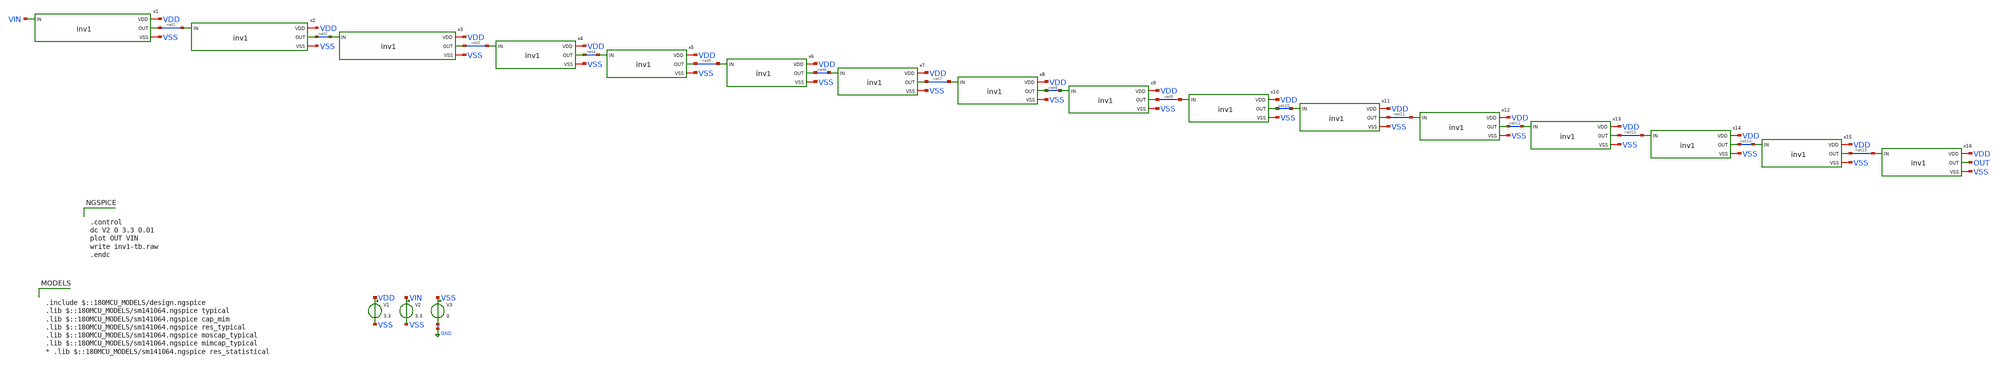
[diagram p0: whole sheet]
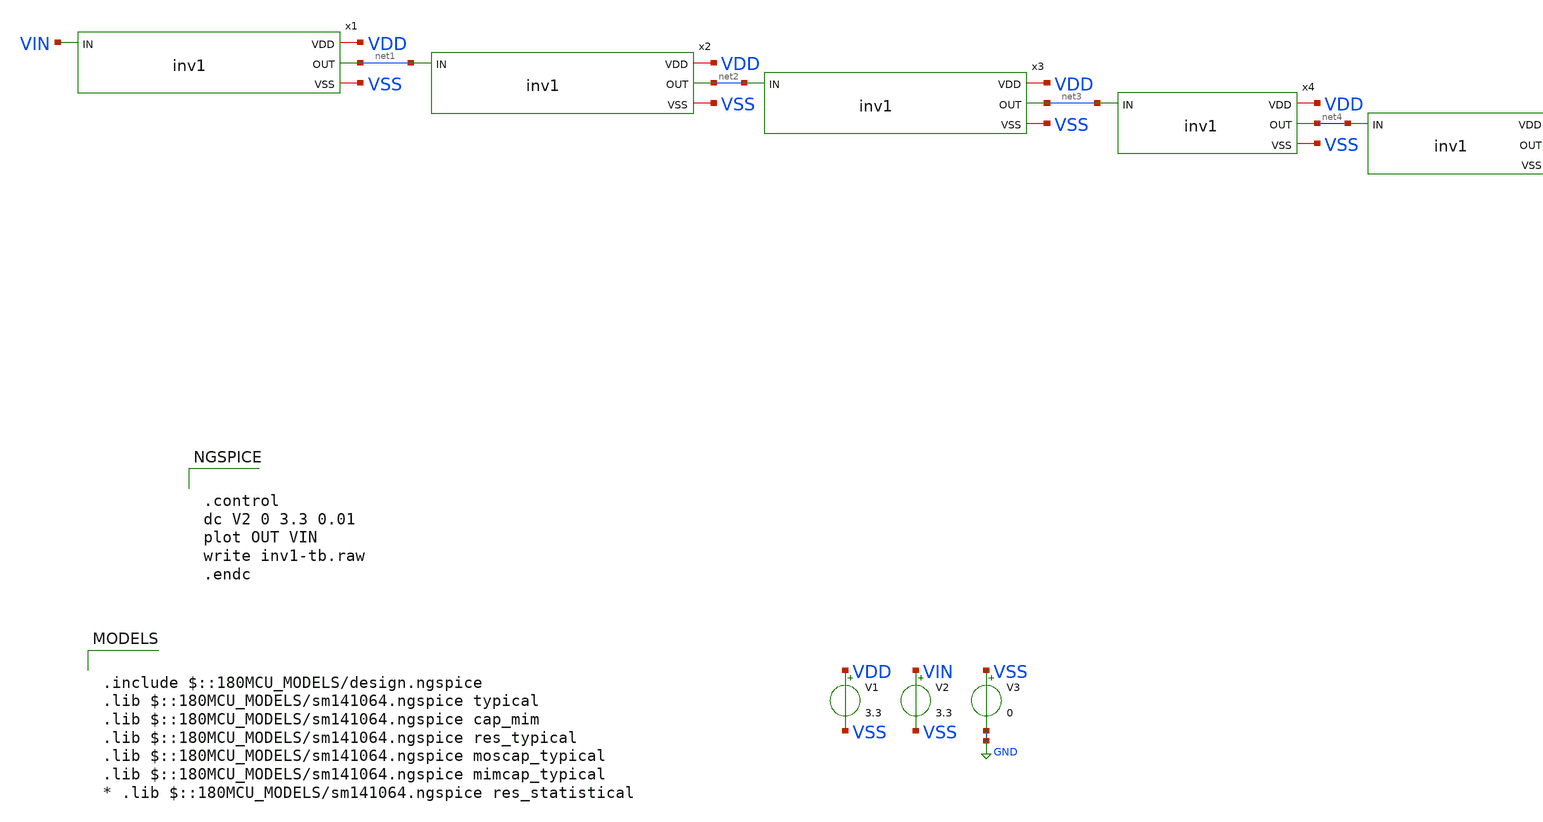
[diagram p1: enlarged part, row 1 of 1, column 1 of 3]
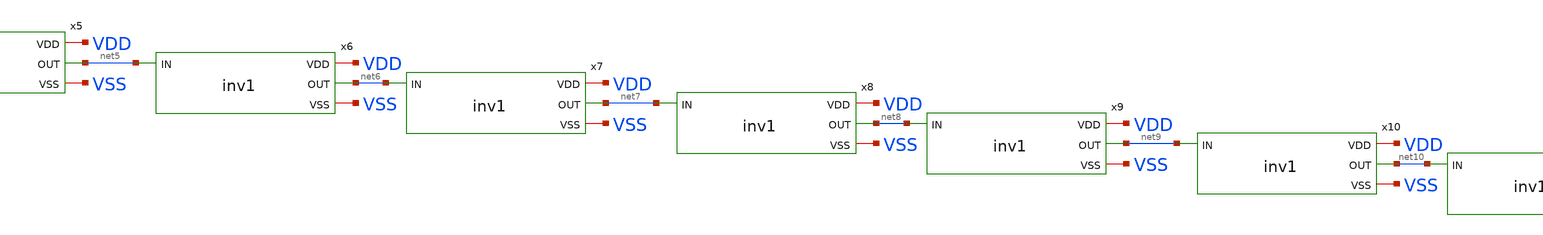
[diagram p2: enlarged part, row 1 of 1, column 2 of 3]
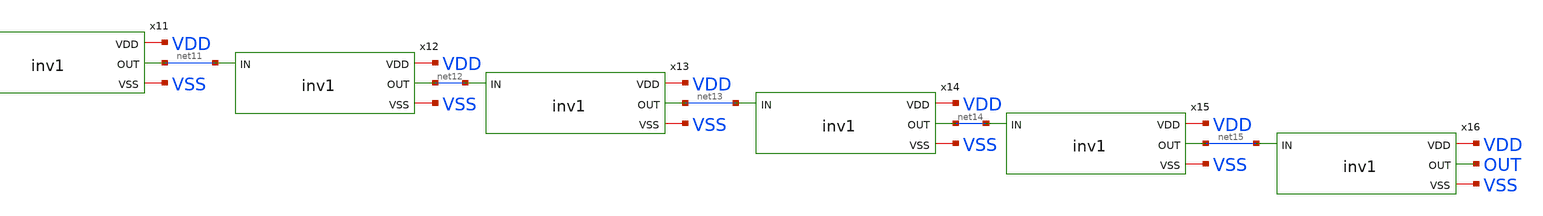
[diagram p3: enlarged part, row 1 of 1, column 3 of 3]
** sch_path: w1_advanced-foundation/w1_task/w1_inv-ring/ring-oscillator.sch
**.subckt ring-oscillator
x1 VDD VIN net1 VSS inv1
x2 VDD net1 net2 VSS inv1
x3 VDD net2 net3 VSS inv1
x4 VDD net3 net4 VSS inv1
x5 VDD net4 net5 VSS inv1
x6 VDD net5 net6 VSS inv1
x7 VDD net6 net7 VSS inv1
x8 VDD net7 net8 VSS inv1
x9 VDD net8 net9 VSS inv1
x10 VDD net9 net10 VSS inv1
x11 VDD net10 net11 VSS inv1
x12 VDD net11 net12 VSS inv1
x13 VDD net12 net13 VSS inv1
x14 VDD net13 net14 VSS inv1
x15 VDD net14 net15 VSS inv1
x16 VDD net15 OUT VSS inv1
V1 VDD VSS 3.3
V2 VIN VSS 3.3
V3 VSS GND 0
**** begin user architecture code

.include $::180MCU_MODELS/design.ngspice
.lib $::180MCU_MODELS/sm141064.ngspice typical
.lib $::180MCU_MODELS/sm141064.ngspice cap_mim
.lib $::180MCU_MODELS/sm141064.ngspice res_typical
.lib $::180MCU_MODELS/sm141064.ngspice moscap_typical
.lib $::180MCU_MODELS/sm141064.ngspice mimcap_typical
* .lib $::180MCU_MODELS/sm141064.ngspice res_statistical



.control
dc V2 0 3.3 0.01
plot OUT VIN
write inv1-tb.raw
.endc


**** end user architecture code
**.ends

* expanding   symbol:  inv1.sym # of pins=4
** sym_path: w1_advanced-foundation/w1_task/w1_inv-ring/inv1.sym
** sch_path: w1_advanced-foundation/w1_task/w1_inv-ring/inv1.sch
.subckt inv1 VDD IN OUT VSS
*.iopin VDD
*.iopin VSS
*.ipin IN
*.opin OUT
XM2 OUT IN VDD VDD pfet_03v3 L=0.28u W=0.22u nf=1 ad='int((nf+1)/2) * W/nf * 0.18u' as='int((nf+2)/2) * W/nf * 0.18u'
+ pd='2*int((nf+1)/2) * (W/nf + 0.18u)' ps='2*int((nf+2)/2) * (W/nf + 0.18u)' nrd='0.18u / W' nrs='0.18u / W'
+ sa=0 sb=0 sd=0 m=3
XM1 OUT IN VSS VSS nfet_03v3 L=0.28u W=0.22u nf=1 ad='int((nf+1)/2) * W/nf * 0.18u' as='int((nf+2)/2) * W/nf * 0.18u'
+ pd='2*int((nf+1)/2) * (W/nf + 0.18u)' ps='2*int((nf+2)/2) * (W/nf + 0.18u)' nrd='0.18u / W' nrs='0.18u / W'
+ sa=0 sb=0 sd=0 m=1
.ends

.GLOBAL GND
.end
